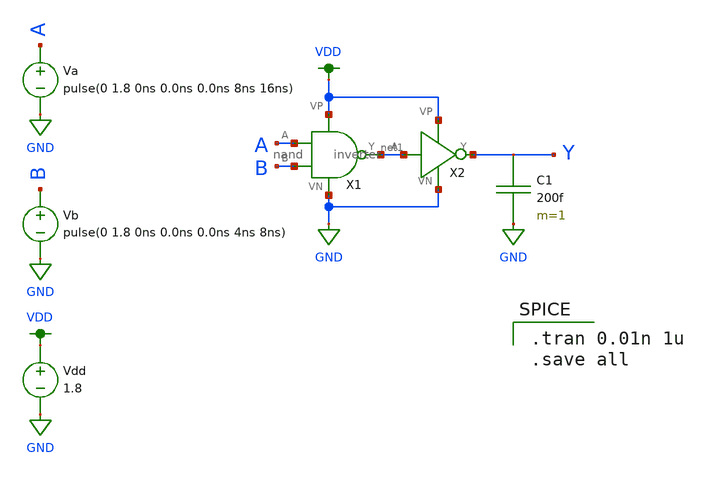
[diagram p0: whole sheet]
** sch_path: mp1/and/and_test_harness.sch
**.subckt and_test_harness
X1 A B net1 VDD GND nand
X2 net1 Y VDD GND inverter
Vb B GND pulse(0 1.8 0ns 0.0ns 0.0ns 4ns 8ns)
Va A GND pulse(0 1.8 0ns 0.0ns 0.0ns 8ns 16ns)
Vdd VDD GND 1.8
C1 Y GND 200f m=1
**** begin user architecture code

.option wnflag=1
.lib ~/skywater/skywater-pdk/libraries/sky130_fd_pr_ngspice/latest/models/sky130.lib.spice tt


.tran 0.01n 1u
.save all

**** end user architecture code
**.ends

* expanding   symbol:  /home/madvlsi/Documents/mp1/nand/nand.sym # of pins=5
** sym_path: mp1/nand/nand.sym
** sch_path: mp1/nand/nand.sch
.subckt nand A B Y VP VN
*.ipin A
*.ipin B
*.opin Y
*.iopin VP
*.iopin VN
XM1 Y A VP VP sky130_fd_pr__pfet_01v8 L=0.15 W=1 nf=1 ad='int((nf+1)/2) * W/nf * 0.29' as='int((nf+2)/2) * W/nf * 0.29'
+ pd='2*int((nf+1)/2) * (W/nf + 0.29)' ps='2*int((nf+2)/2) * (W/nf + 0.29)' nrd='0.29 / W' nrs='0.29 / W'
+ sa=0 sb=0 sd=0 mult=1 m=1
XM2 Y B VP VP sky130_fd_pr__pfet_01v8 L=0.15 W=1 nf=1 ad='int((nf+1)/2) * W/nf * 0.29' as='int((nf+2)/2) * W/nf * 0.29'
+ pd='2*int((nf+1)/2) * (W/nf + 0.29)' ps='2*int((nf+2)/2) * (W/nf + 0.29)' nrd='0.29 / W' nrs='0.29 / W'
+ sa=0 sb=0 sd=0 mult=1 m=1
XM3 Y A net1 VN sky130_fd_pr__nfet_01v8 L=0.15 W=1 nf=1 ad='int((nf+1)/2) * W/nf * 0.29' as='int((nf+2)/2) * W/nf * 0.29'
+ pd='2*int((nf+1)/2) * (W/nf + 0.29)' ps='2*int((nf+2)/2) * (W/nf + 0.29)' nrd='0.29 / W' nrs='0.29 / W'
+ sa=0 sb=0 sd=0 mult=1 m=1
XM4 net1 B VN VN sky130_fd_pr__nfet_01v8 L=0.15 W=1 nf=1 ad='int((nf+1)/2) * W/nf * 0.29' as='int((nf+2)/2) * W/nf * 0.29'
+ pd='2*int((nf+1)/2) * (W/nf + 0.29)' ps='2*int((nf+2)/2) * (W/nf + 0.29)' nrd='0.29 / W' nrs='0.29 / W'
+ sa=0 sb=0 sd=0 mult=1 m=1
.ends


* expanding   symbol:  /home/madvlsi/Documents/mp1/inverter/inverter.sym # of pins=4
** sym_path: mp1/inverter/inverter.sym
** sch_path: mp1/inverter/inverter.sch
.subckt inverter A Y VP VN
*.ipin A
*.iopin VP
*.iopin VN
*.opin Y
XM1 Y A VN VN sky130_fd_pr__nfet_01v8 L=0.15 W=1 nf=1 ad='int((nf+1)/2) * W/nf * 0.29' as='int((nf+2)/2) * W/nf * 0.29'
+ pd='2*int((nf+1)/2) * (W/nf + 0.29)' ps='2*int((nf+2)/2) * (W/nf + 0.29)' nrd='0.29 / W' nrs='0.29 / W'
+ sa=0 sb=0 sd=0 mult=1 m=1
XM2 Y A VP VP sky130_fd_pr__pfet_01v8 L=0.15 W=1 nf=1 ad='int((nf+1)/2) * W/nf * 0.29' as='int((nf+2)/2) * W/nf * 0.29'
+ pd='2*int((nf+1)/2) * (W/nf + 0.29)' ps='2*int((nf+2)/2) * (W/nf + 0.29)' nrd='0.29 / W' nrs='0.29 / W'
+ sa=0 sb=0 sd=0 mult=1 m=1
.ends

.GLOBAL VDD
.GLOBAL GND
.end
